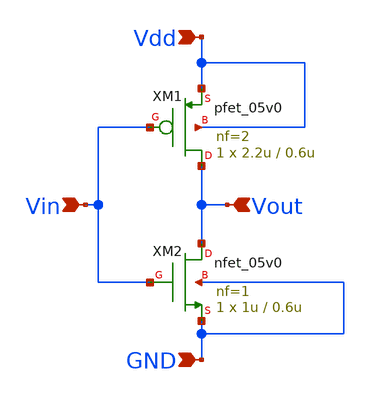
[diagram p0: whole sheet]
** sch_path: MG_decoder/MG_not_gate.sch
**.subckt MG_not_gate Vdd GND Vin Vout
*.ipin Vdd
*.ipin GND
*.ipin Vin
*.ipin Vout
XM1 Vout Vin Vdd Vdd pfet_05v0 L=0.6u W=2.2u nf=2 ad='int((nf+1)/2) * W/nf * 0.18u' as='int((nf+2)/2) * W/nf * 0.18u'
+ pd='2*int((nf+1)/2) * (W/nf + 0.18u)' ps='2*int((nf+2)/2) * (W/nf + 0.18u)' nrd='0.18u / W' nrs='0.18u / W'
+ sa=0 sb=0 sd=0 m=1
XM2 Vout Vin GND GND nfet_05v0 L=0.6u W=1u nf=1 ad='int((nf+1)/2) * W/nf * 0.18u' as='int((nf+2)/2) * W/nf * 0.18u'
+ pd='2*int((nf+1)/2) * (W/nf + 0.18u)' ps='2*int((nf+2)/2) * (W/nf + 0.18u)' nrd='0.18u / W' nrs='0.18u / W'
+ sa=0 sb=0 sd=0 m=1
**.ends
.end
